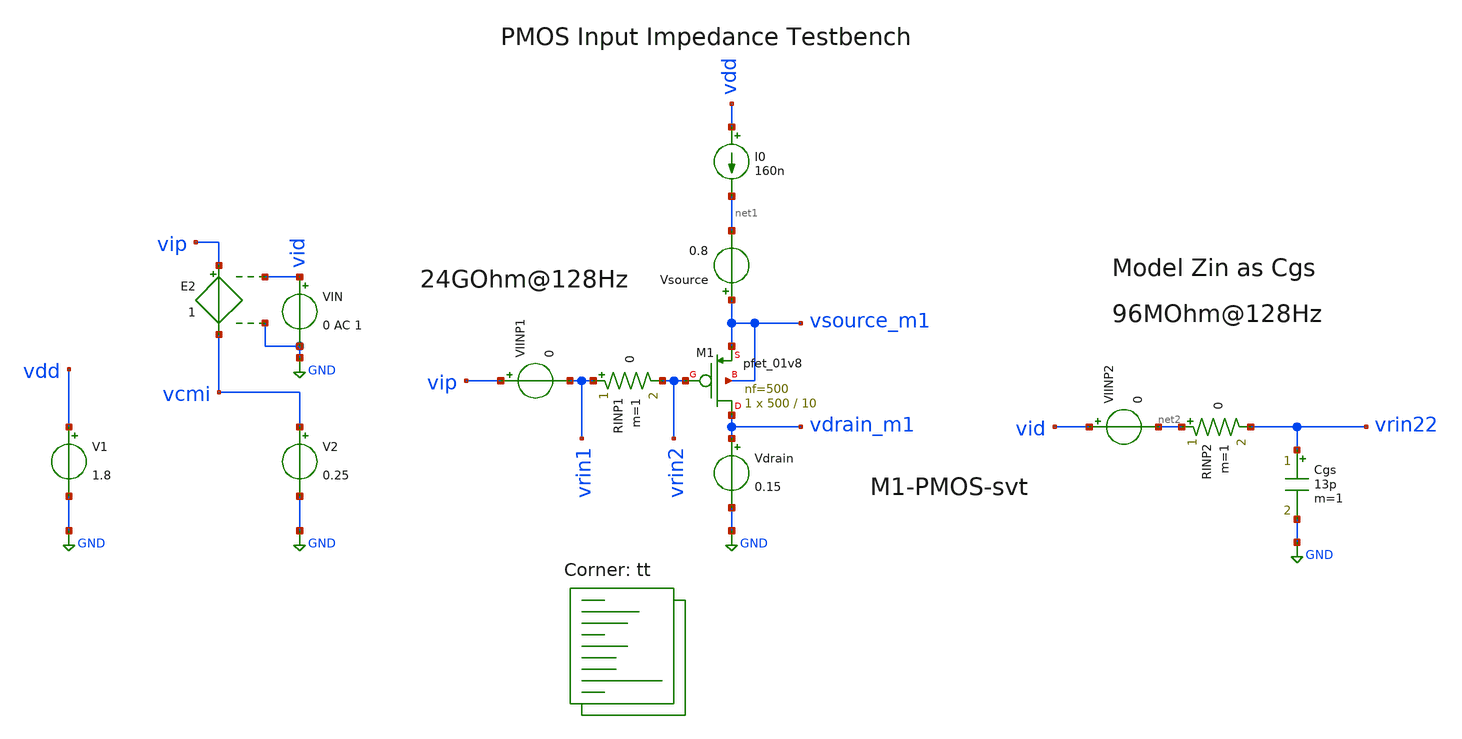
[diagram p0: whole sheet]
** sch_path: circuit-level/xschem/pmos_1v8_svt_zin.sch
**.subckt pmos_1v8_svt_zin
V1 vdd GND 1.8
V2 vcmi GND 0.25
E2 vip vcmi vid GND 1
VIN vid GND 0 AC 1
XM1 vdrain_m1 vrin2 vsource_m1 vsource_m1 sky130_fd_pr__pfet_01v8 L=10 W=500 nf=500 ad='int((nf+1)/2) * W/nf * 0.29'
+ as='int((nf+2)/2) * W/nf * 0.29' pd='2*int((nf+1)/2) * (W/nf + 0.29)' ps='2*int((nf+2)/2) * (W/nf + 0.29)'
+ nrd='0.29 / W' nrs='0.29 / W' sa=0 sb=0 sd=0 mult=1 m=1
RINP1 vrin1 vrin2 0 m=1
VIINP1 vip vrin1 0
Vsource vsource_m1 net1 0.8
Vdrain vdrain_m1 GND 0.15
I0 vdd net1 160n
RINP2 net2 vrin22 0 m=1
Cgs vrin22 GND 13p m=1
VIINP2 vid net2 0
**** begin user architecture code
.lib $::SKYWATER_MODELS/sky130.lib.spice tt


.options savecurrents
.control
save all

save @m.xm1.msky130_fd_pr__pfet_01v8[id]
save @m.xm1.msky130_fd_pr__pfet_01v8[vth]
save @m.xm1.msky130_fd_pr__pfet_01v8[vgs]
save @m.xm1.msky130_fd_pr__pfet_01v8[vds]
save @m.xm1.msky130_fd_pr__pfet_01v8[vdsat]
save @m.xm1.msky130_fd_pr__pfet_01v8[gm]
save @m.xm1.msky130_fd_pr__pfet_01v8[gds]
save @m.xm1.msky130_fd_pr__pfet_01v8[cgs]
save @m.xm1.msky130_fd_pr__pfet_01v8[cgd]
save @m.xm1.msky130_fd_pr__pfet_01v8[cgg]
save @m.xm1.msky130_fd_pr__pfet_01v8[csg]

let f_sig = 128
alter @VIN[SIN] = [ 0 0.1 $&f_sig 0 0 0 ]
alter @VIN[DC] = 0.0

let tstep = 0.01/f_sig
let tstop = 100/f_sig

** Main Simulations
op

ac dec 100 0.1 1e5

** Expected Input Impedance based on Cgs
setplot op1
let cgsm1 = abs(@m.xm1.msky130_fd_pr__pfet_01v8[cgg])
let zin_est = 1/(2*pi*const.f_sig*cgsm1)
alter @rinp2[resistance] = zin_est
alter @cgs[capacitance] = cgsm1

setplot ac1
let zin_m1 = abs(v(vip)/viinp1#branch)
let zin_model = abs(v(vid)/viinp2#branch)
meas ac zin_m1_fsig find zin_m1 when frequency=f_sig
meas ac zin_model_fsig find zin_model when frequency=f_sig
plot vdb(zin_m1) vdb(zin_model)
plot zin_m1 zin_model

alter @rinp1[resistance] = zin_m1_fsig

tran $&tstep $&tstop
setplot tran1

let vrin_m1 = v(vrin1,vrin2)
let vref_m1 = (vip-0.25)/sqrt(2)

let vrin_ref = v(vid,vrin22)
let vref = vid/sqrt(2)

plot vrin_m1 vref_m1
plot vrin_ref vref

setplot ac1
print zin_m1_fsig
print zin_model_fsig

op

remzerovec
write pmos_1v8_svt_zin.raw
.endc

**** end user architecture code
**.ends
.GLOBAL GND
.end
